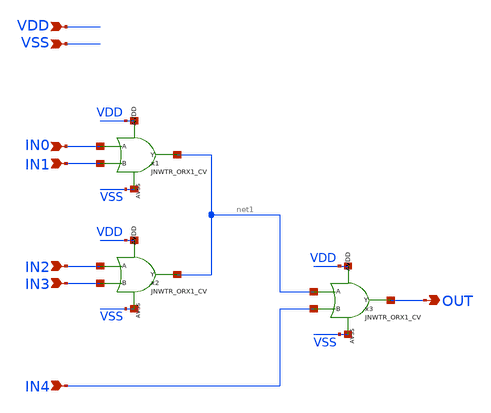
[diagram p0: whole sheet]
** sch_path: design/LELO_TORD_SKY130A/5-input-or-gate.sch
**.subckt 5-input-or-gate IN0 IN1 VDD VSS IN2 IN3 IN4 OUT
*.ipin IN0
*.ipin IN1
*.ipin VDD
*.ipin VSS
*.ipin IN2
*.ipin IN3
*.ipin IN4
*.opin OUT
x1 IN0 IN1 net1 VDD VSS JNWTR_ORX1_CV xoffset=0 yoffset=0 angle=0 M=1
x2 IN2 IN3 net1 VDD VSS JNWTR_ORX1_CV xoffset=0 yoffset=0 angle=0 M=1
x3 net1 IN4 OUT VDD VSS JNWTR_ORX1_CV xoffset=0 yoffset=0 angle=0 M=1
**.ends
.end
